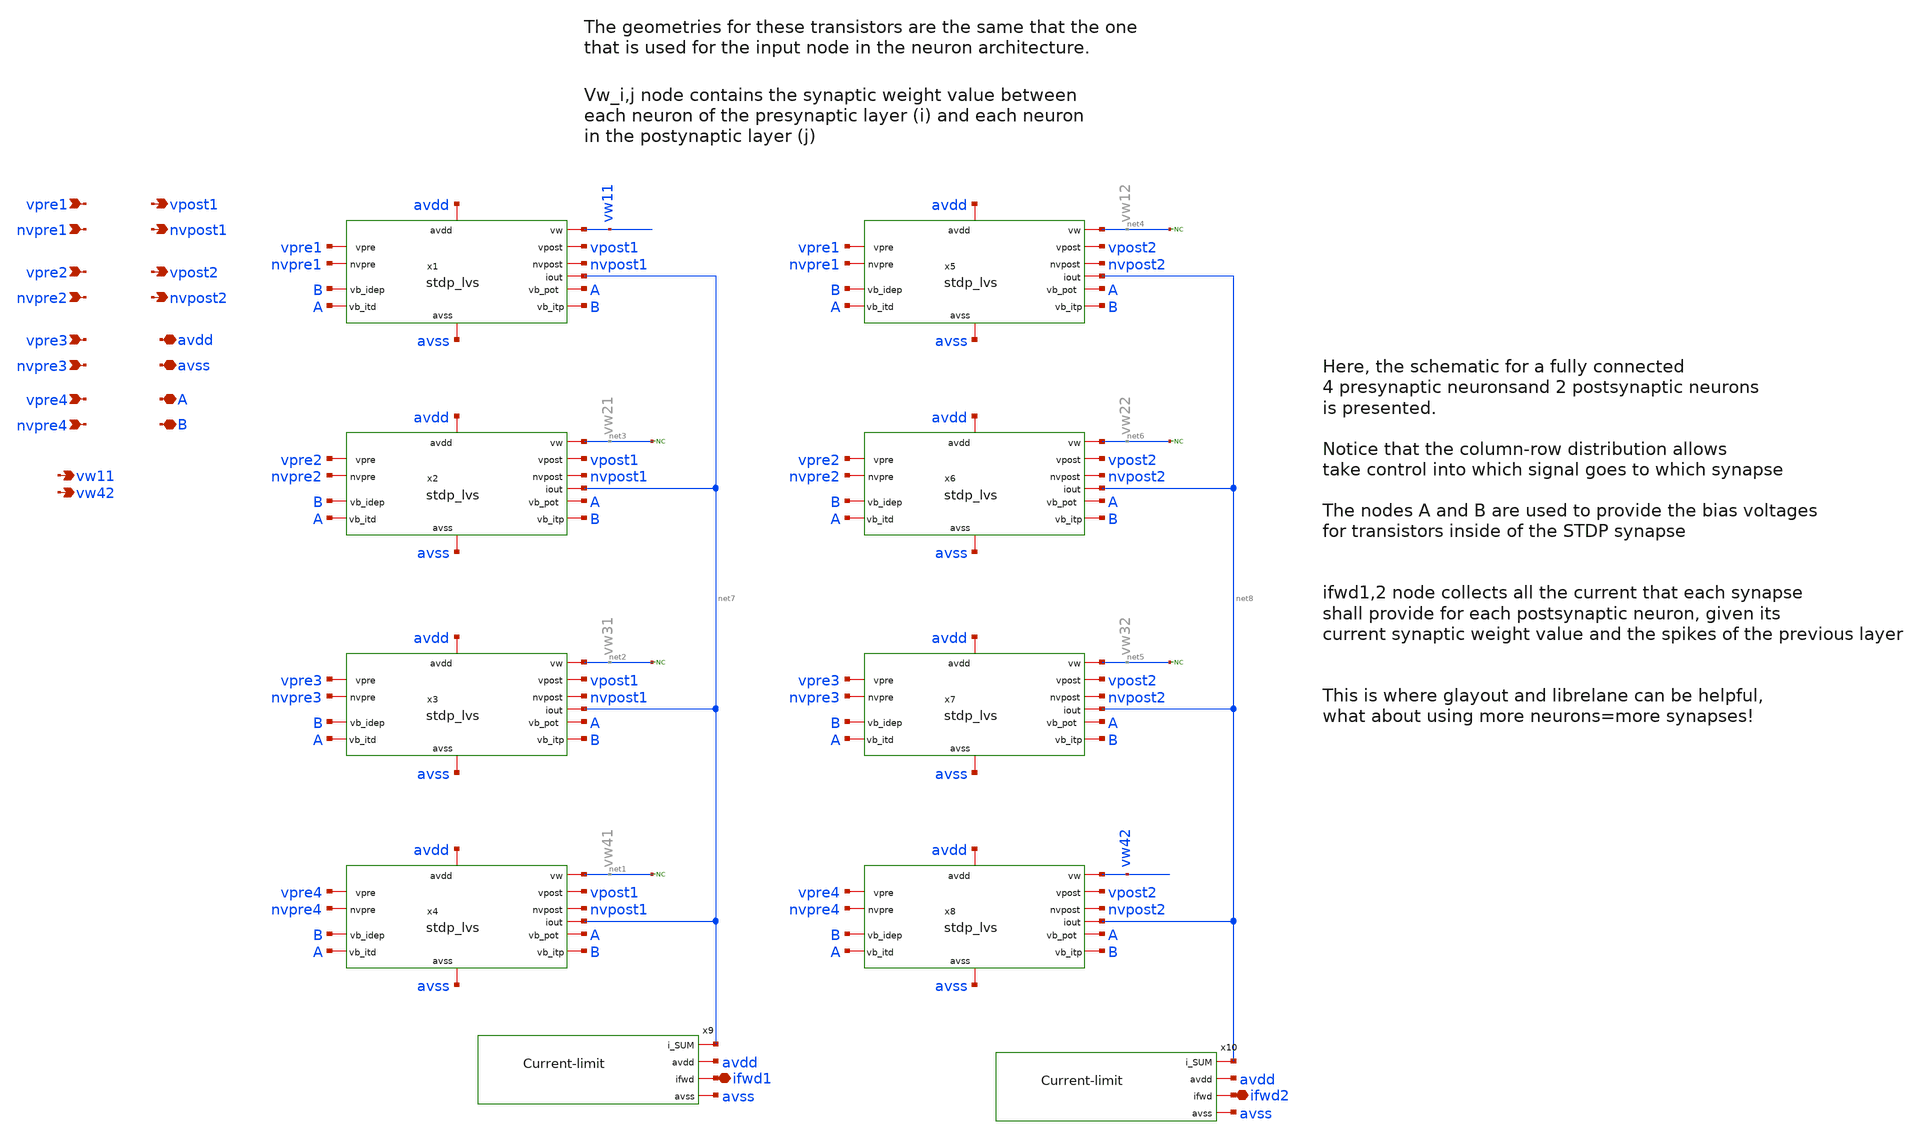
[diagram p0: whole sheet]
** sch_path: designs/libs/snn_analog/stdp/sch/stdp/stdp_4x2_lvs.sch
**.subckt stdp_4x2_lvs ifwd1 ifwd2 vpre1 nvpre1 vpre2 nvpre2 vpre3 nvpre3 vpre4 nvpre4 vpost1
*+ nvpost1 vpost2 nvpost2 avdd avss A B vw11 vw42
*.iopin ifwd1
*.iopin ifwd2
*.ipin vpre1
*.ipin nvpre1
*.ipin vpre2
*.ipin nvpre2
*.ipin vpre3
*.ipin nvpre3
*.ipin vpre4
*.ipin nvpre4
*.opin vpost1
*.opin nvpost1
*.opin vpost2
*.opin nvpost2
*.iopin avdd
*.iopin avss
*.iopin A
*.iopin B
*.opin vw11
*.opin vw42
x1 avdd avss nvpre1 nvpost1 vpre1 vpost1 A B B A vw11 net7 stdp_lvs
x2 avdd avss nvpre2 nvpost1 vpre2 vpost1 A B B A net3 net7 stdp_lvs
x3 avdd avss nvpre3 nvpost1 vpre3 vpost1 A B B A net2 net7 stdp_lvs
x4 avdd avss nvpre4 nvpost1 vpre4 vpost1 A B B A net1 net7 stdp_lvs
x5 avdd avss nvpre1 nvpost2 vpre1 vpost2 A B B A net4 net8 stdp_lvs
x6 avdd avss nvpre2 nvpost2 vpre2 vpost2 A B B A net6 net8 stdp_lvs
x7 avdd avss nvpre3 nvpost2 vpre3 vpost2 A B B A net5 net8 stdp_lvs
x8 avdd avss nvpre4 nvpost2 vpre4 vpost2 A B B A vw42 net8 stdp_lvs
x9 net7 avdd ifwd1 avss Current-limit
x10 net8 avdd ifwd2 avss Current-limit
* noconn #net3
* noconn #net4
* noconn #net6
* noconn #net5
* noconn #net2
* noconn #net1
**.ends
.end
